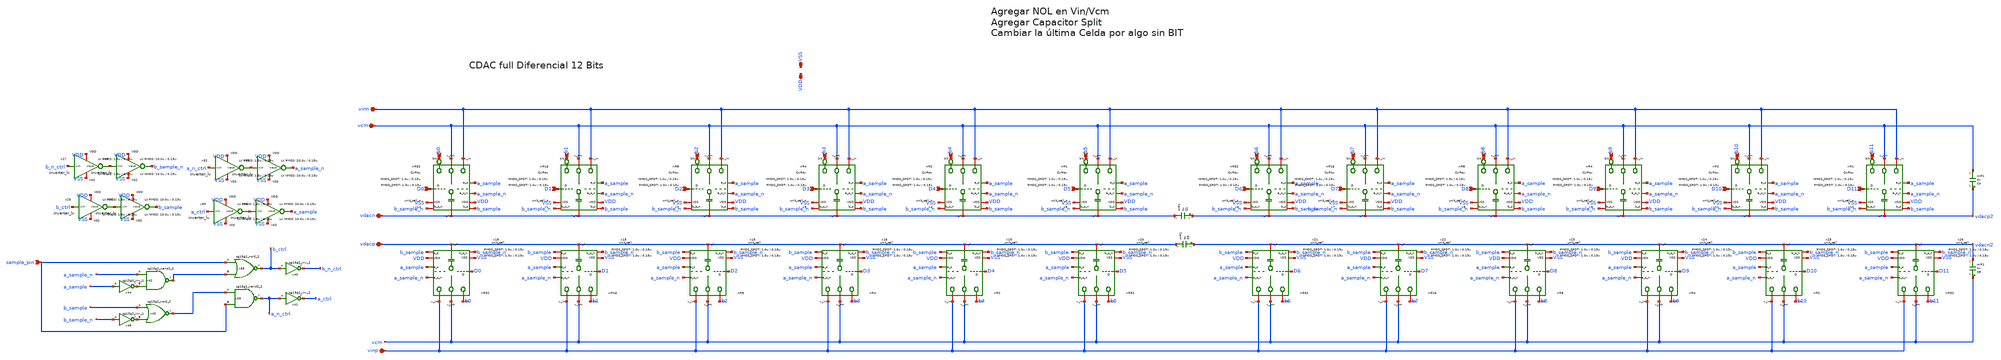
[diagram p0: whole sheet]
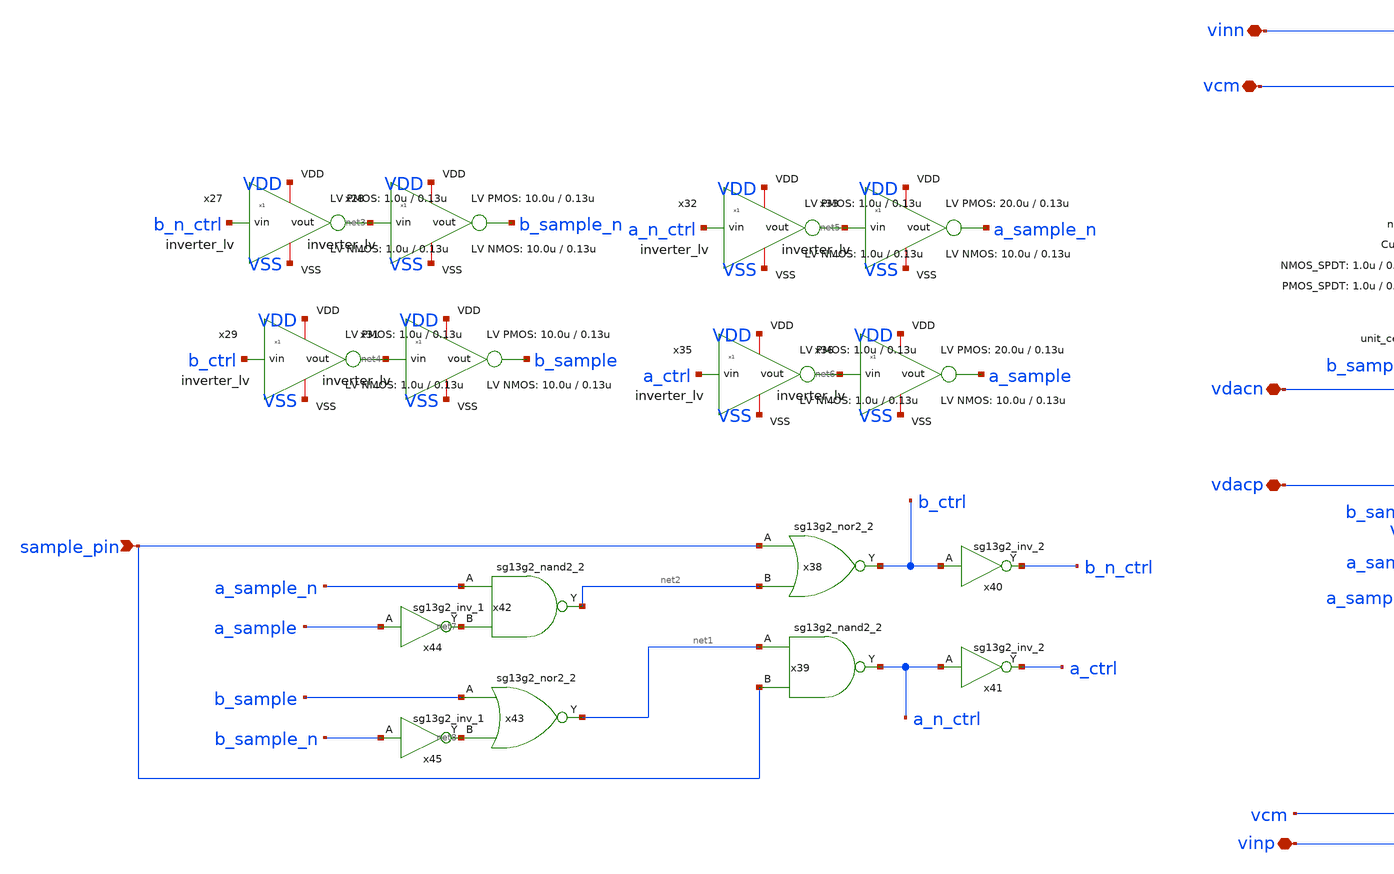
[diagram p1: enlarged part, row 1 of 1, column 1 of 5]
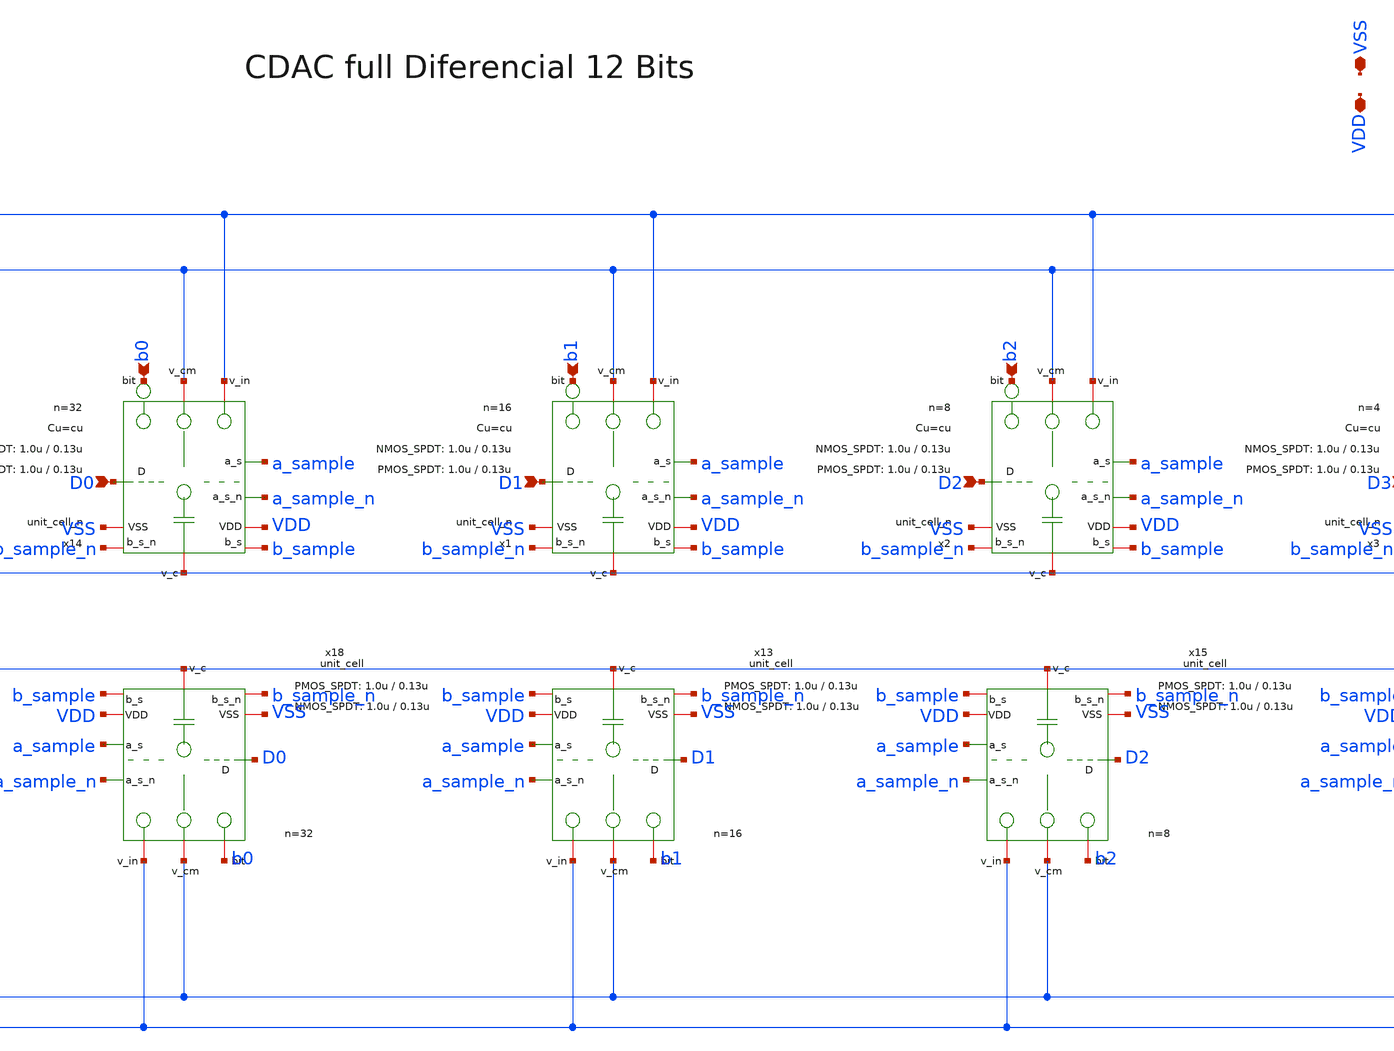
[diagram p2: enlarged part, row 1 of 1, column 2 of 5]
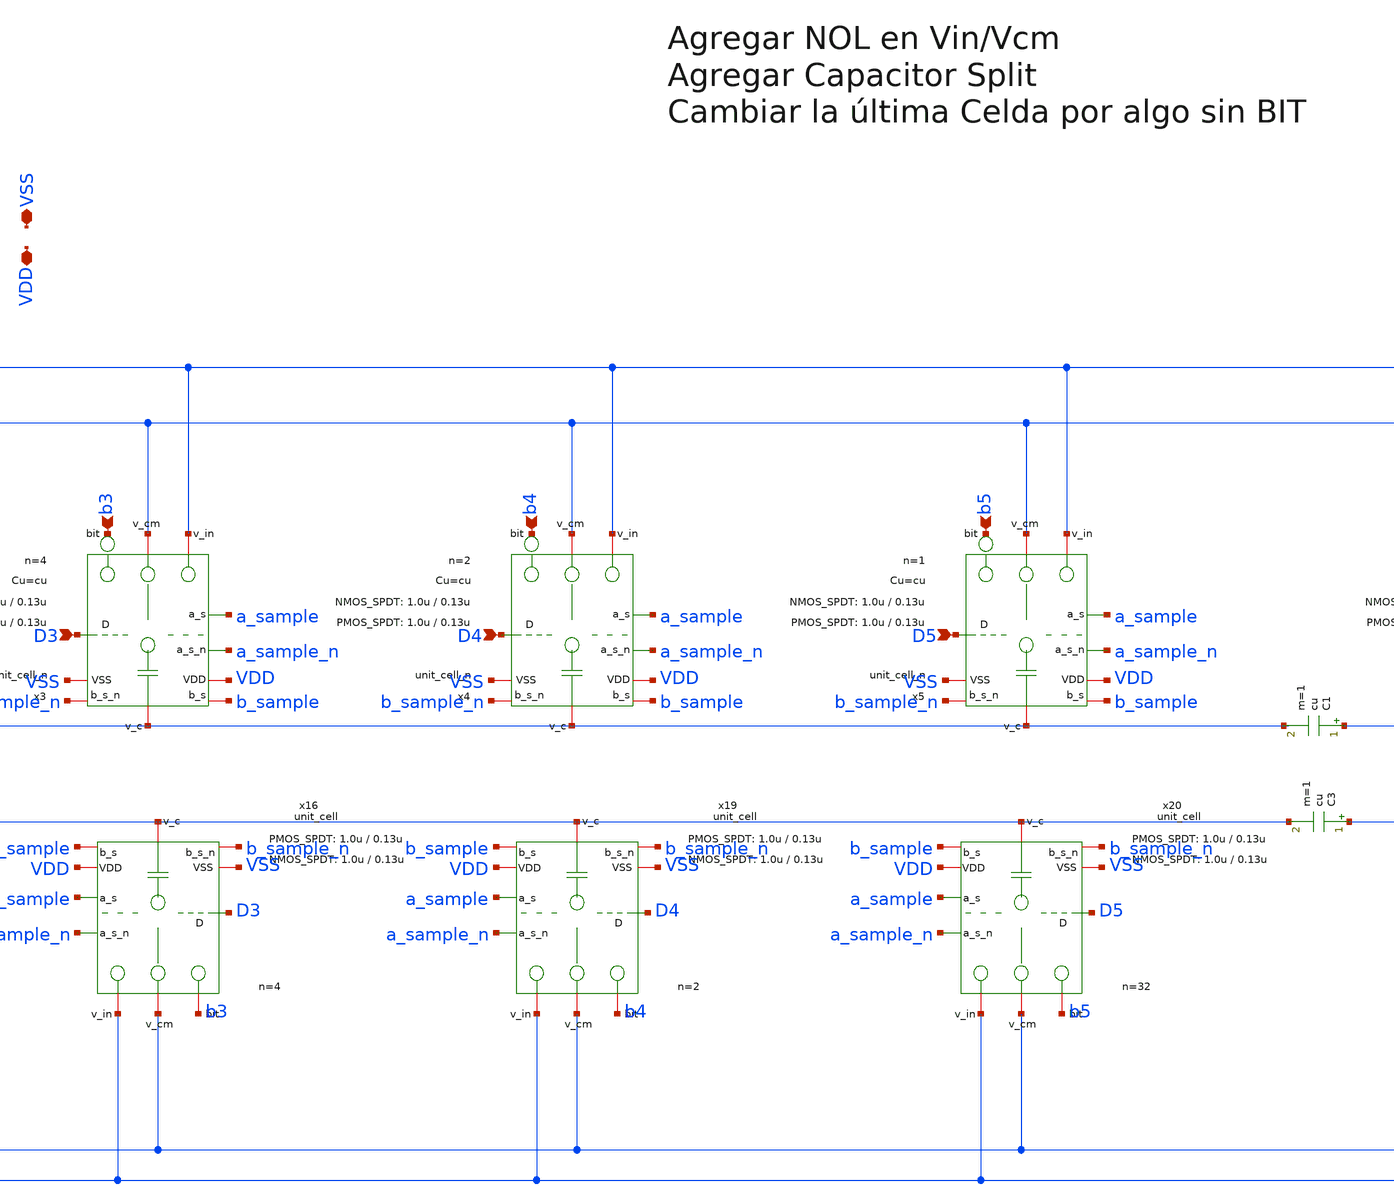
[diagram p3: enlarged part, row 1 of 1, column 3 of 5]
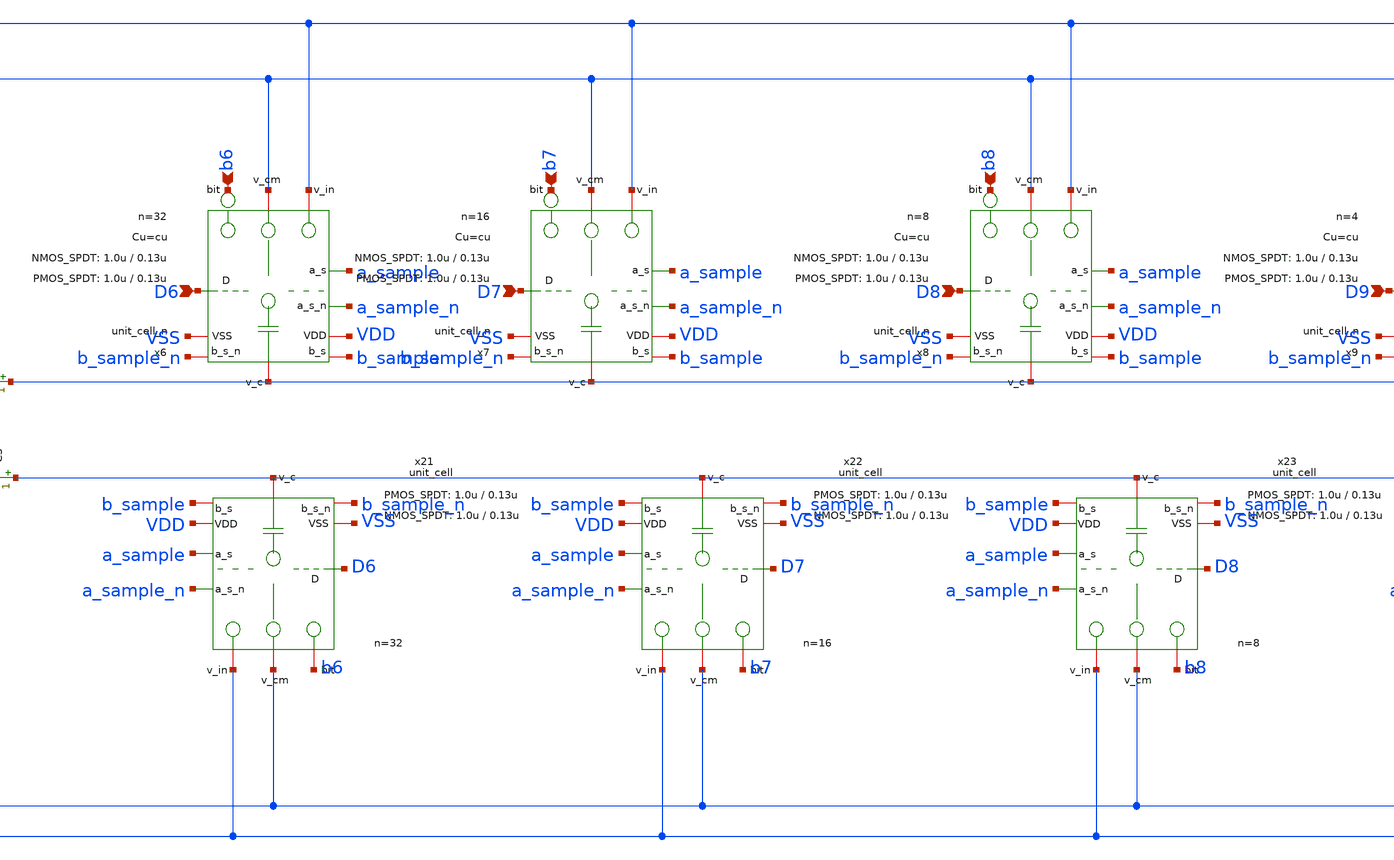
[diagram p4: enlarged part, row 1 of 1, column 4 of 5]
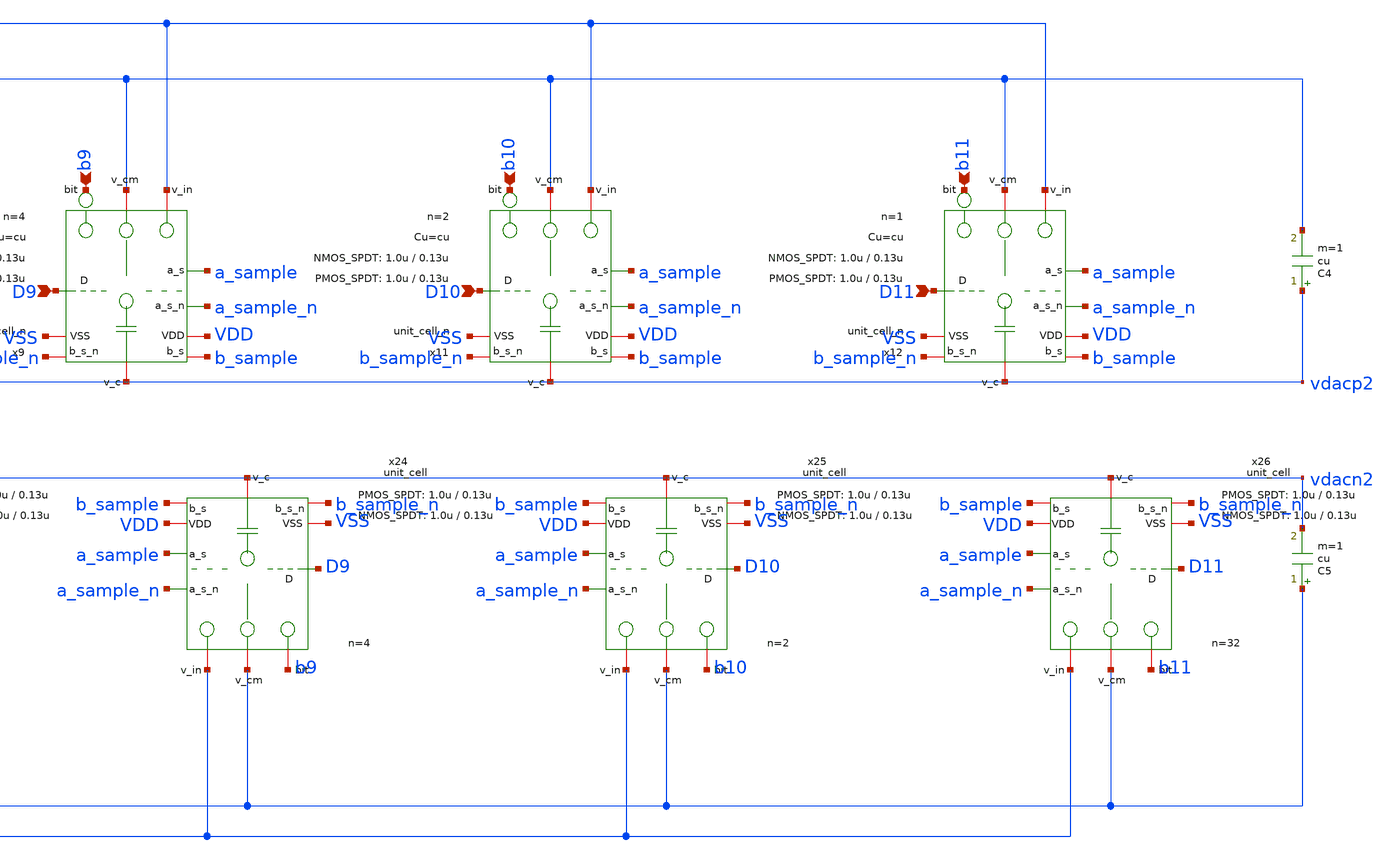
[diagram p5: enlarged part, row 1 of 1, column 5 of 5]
** sch_path: xschem/dac_icms_cell_ideal/dac.sch
* IHP-GmbH/IHP-Open-PDK/ihp-sg13g2/libs.tech/xschem/sg13g2_stdcells/sg13g2_inv_2.sch:
* Copyright 2023 IHP PDK Authors
* Licensed under the Apache License, Version 2.0 (the "License");
**.subckt dac D0 b0 vinp vcm sample_pin vinn vdacp vdacn VSS VDD D1 b1 D2 b2 D3 b3 D4 b4 D5 b5 D6 b6
*+ D7 b7 D8 b8 D9 b9 D10 b10 D11 b11
*.ipin D0
*.ipin b0
*.iopin vinp
*.iopin vcm
*.ipin sample_pin
*.iopin vinn
*.iopin vdacp
*.iopin vdacn
*.iopin VSS
*.iopin VDD
*.ipin D1
*.ipin b1
*.ipin D2
*.ipin b2
*.ipin D3
*.ipin b3
*.ipin D4
*.ipin b4
*.ipin D5
*.ipin b5
*.ipin D6
*.ipin b6
*.ipin D7
*.ipin b7
*.ipin D8
*.ipin b8
*.ipin D9
*.ipin b9
*.ipin D10
*.ipin b10
*.ipin D11
*.ipin b11
x14 VDD D0 VSS vdacn b0 vcm vinn a_sample a_sample_n b_sample b_sample_n unit_cell_n W_P=
+ L_P_SPDT=0.13u W_N= L_N_SPDT=0.13u Cu=cu n=32
x18 VDD D0 VSS vdacp b0 vcm vinp a_sample a_sample_n b_sample b_sample_n unit_cell W_P_SPDT=1.0u
+ L_P_SPDT=0.13u W_N_SPDT=1.0u L_N_SPDT=0.13u Cu=cu n=32
C1 vdacp2 vdacn cu m=1
C4 vdacp2 vcm cu m=1
x1 VDD D1 VSS vdacn b1 vcm vinn a_sample a_sample_n b_sample b_sample_n unit_cell_n W_P=
+ L_P_SPDT=0.13u W_N= L_N_SPDT=0.13u Cu=cu n=16
x2 VDD D2 VSS vdacn b2 vcm vinn a_sample a_sample_n b_sample b_sample_n unit_cell_n W_P=
+ L_P_SPDT=0.13u W_N= L_N_SPDT=0.13u Cu=cu n=8
x3 VDD D3 VSS vdacn b3 vcm vinn a_sample a_sample_n b_sample b_sample_n unit_cell_n W_P=
+ L_P_SPDT=0.13u W_N= L_N_SPDT=0.13u Cu=cu n=4
x4 VDD D4 VSS vdacn b4 vcm vinn a_sample a_sample_n b_sample b_sample_n unit_cell_n W_P=
+ L_P_SPDT=0.13u W_N= L_N_SPDT=0.13u Cu=cu n=2
x5 VDD D5 VSS vdacn b5 vcm vinn a_sample a_sample_n b_sample b_sample_n unit_cell_n W_P=
+ L_P_SPDT=0.13u W_N= L_N_SPDT=0.13u Cu=cu n=1
x6 VDD D6 VSS vdacp2 b6 vcm vinn a_sample a_sample_n b_sample b_sample_n unit_cell_n W_P=
+ L_P_SPDT=0.13u W_N= L_N_SPDT=0.13u Cu=cu n=32
x7 VDD D7 VSS vdacp2 b7 vcm vinn a_sample a_sample_n b_sample b_sample_n unit_cell_n W_P=
+ L_P_SPDT=0.13u W_N= L_N_SPDT=0.13u Cu=cu n=16
x8 VDD D8 VSS vdacp2 b8 vcm vinn a_sample a_sample_n b_sample b_sample_n unit_cell_n W_P=
+ L_P_SPDT=0.13u W_N= L_N_SPDT=0.13u Cu=cu n=8
x9 VDD D9 VSS vdacp2 b9 vcm vinn a_sample a_sample_n b_sample b_sample_n unit_cell_n W_P=
+ L_P_SPDT=0.13u W_N= L_N_SPDT=0.13u Cu=cu n=4
x11 VDD D10 VSS vdacp2 b10 vcm vinn a_sample a_sample_n b_sample b_sample_n unit_cell_n W_P=
+ L_P_SPDT=0.13u W_N= L_N_SPDT=0.13u Cu=cu n=2
x12 VDD D11 VSS vdacp2 b11 vcm vinn a_sample a_sample_n b_sample b_sample_n unit_cell_n W_P=
+ L_P_SPDT=0.13u W_N= L_N_SPDT=0.13u Cu=cu n=1
x13 VDD D1 VSS vdacp b1 vcm vinp a_sample a_sample_n b_sample b_sample_n unit_cell W_P_SPDT=1.0u
+ L_P_SPDT=0.13u W_N_SPDT=1.0u L_N_SPDT=0.13u Cu=cu n=16
x15 VDD D2 VSS vdacp b2 vcm vinp a_sample a_sample_n b_sample b_sample_n unit_cell W_P_SPDT=1.0u
+ L_P_SPDT=0.13u W_N_SPDT=1.0u L_N_SPDT=0.13u Cu=cu n=8
x16 VDD D3 VSS vdacp b3 vcm vinp a_sample a_sample_n b_sample b_sample_n unit_cell W_P_SPDT=1.0u
+ L_P_SPDT=0.13u W_N_SPDT=1.0u L_N_SPDT=0.13u Cu=cu n=4
x19 VDD D4 VSS vdacp b4 vcm vinp a_sample a_sample_n b_sample b_sample_n unit_cell W_P_SPDT=1.0u
+ L_P_SPDT=0.13u W_N_SPDT=1.0u L_N_SPDT=0.13u Cu=cu n=2
x20 VDD D5 VSS vdacp b5 vcm vinp a_sample a_sample_n b_sample b_sample_n unit_cell W_P_SPDT=1.0u
+ L_P_SPDT=0.13u W_N_SPDT=1.0u L_N_SPDT=0.13u Cu=cu n=32
C3 vdacn2 vdacp cu m=1
x21 VDD D6 VSS vdacn2 b6 vcm vinp a_sample a_sample_n b_sample b_sample_n unit_cell W_P_SPDT=1.0u
+ L_P_SPDT=0.13u W_N_SPDT=1.0u L_N_SPDT=0.13u Cu=cu n=32
x22 VDD D7 VSS vdacn2 b7 vcm vinp a_sample a_sample_n b_sample b_sample_n unit_cell W_P_SPDT=1.0u
+ L_P_SPDT=0.13u W_N_SPDT=1.0u L_N_SPDT=0.13u Cu=cu n=16
x23 VDD D8 VSS vdacn2 b8 vcm vinp a_sample a_sample_n b_sample b_sample_n unit_cell W_P_SPDT=1.0u
+ L_P_SPDT=0.13u W_N_SPDT=1.0u L_N_SPDT=0.13u Cu=cu n=8
x24 VDD D9 VSS vdacn2 b9 vcm vinp a_sample a_sample_n b_sample b_sample_n unit_cell W_P_SPDT=1.0u
+ L_P_SPDT=0.13u W_N_SPDT=1.0u L_N_SPDT=0.13u Cu=cu n=4
x25 VDD D10 VSS vdacn2 b10 vcm vinp a_sample a_sample_n b_sample b_sample_n unit_cell W_P_SPDT=1.0u
+ L_P_SPDT=0.13u W_N_SPDT=1.0u L_N_SPDT=0.13u Cu=cu n=2
x26 VDD D11 VSS vdacn2 b11 vcm vinp a_sample a_sample_n b_sample b_sample_n unit_cell W_P_SPDT=1.0u
+ L_P_SPDT=0.13u W_N_SPDT=1.0u L_N_SPDT=0.13u Cu=cu n=32
C5 vcm vdacn2 cu m=1
x27 VDD b_n_ctrl net3 VSS inverter_lv W_P=1.0u L_P=0.13u W_N=1.0u L_N=0.13u N_C=1
x28 VDD net3 b_sample_n VSS inverter_lv W_P=10.0u L_P=0.13u W_N=10.0u L_N=0.13u N_C=1
x29 VDD b_ctrl net4 VSS inverter_lv W_P=1.0u L_P=0.13u W_N=1.0u L_N=0.13u N_C=1
x31 VDD net4 b_sample VSS inverter_lv W_P=10.0u L_P=0.13u W_N=10.0u L_N=0.13u N_C=1
x32 VDD a_n_ctrl net5 VSS inverter_lv W_P=1.0u L_P=0.13u W_N=1.0u L_N=0.13u N_C=1
x33 VDD net5 a_sample_n VSS inverter_lv W_P=20.0u L_P=0.13u W_N=10.0u L_N=0.13u N_C=1
x35 VDD a_ctrl net6 VSS inverter_lv W_P=1.0u L_P=0.13u W_N=1.0u L_N=0.13u N_C=1
x36 VDD net6 a_sample VSS inverter_lv W_P=20.0u L_P=0.13u W_N=10.0u L_N=0.13u N_C=1
x38 b_ctrl sample_pin net2 VDD VSS sg13g2_nor2_2
x39 a_n_ctrl net1 sample_pin VDD VSS sg13g2_nand2_2
x40 b_n_ctrl b_ctrl VDD VSS sg13g2_inv_2
x41 a_ctrl a_n_ctrl VDD VSS sg13g2_inv_2
x42 net2 a_sample_n net7 VDD VSS sg13g2_nand2_2
x43 net1 b_sample net8 VDD VSS sg13g2_nor2_2
x44 net7 a_sample VDD VSS sg13g2_inv_1
x45 net8 b_sample_n VDD VSS sg13g2_inv_1
**.ends

* expanding   symbol:  dac_icms_cell/unit_cell_n.sym # of pins=11
** sym_path: xschem/dac_icms_cell/unit_cell_n.sym
** sch_path: xschem/dac_icms_cell/unit_cell_n.sch
.subckt unit_cell_n VDD d VSS v_top bit v_cm v_in a_sample a_sample_n b_sample b_sample_n
+  W_P_SPDT=1.0u L_P_SPDT=0.13u W_N_SPDT=1.0u L_N_SPDT=0.13u Cu=8f n=1
*.iopin VSS
*.iopin v_in
*.ipin d
*.ipin bit
*.iopin v_top
*.iopin v_cm
*.ipin b_sample
*.ipin b_sample_n
*.ipin a_sample
*.ipin a_sample_n
*.iopin VDD
S1 net2 net3 d VSS SW1
C2 net1 v_top Cu m=n
S2 net3 net1 b_sample b_sample_n SW1
S3 v_in net1 b_sample_n b_sample SW1
S4 v_top v_cm a_sample a_sample_n SW1
S5 VDD net2 bit VSS SW1
S6 net2 VSS bitn VSS SW1
S7 net3 v_cm dn VSS SW1
x8 VDD bit bitn VSS inverter_lv W_P=W_P_SPDT L_P=L_P_SPDT W_N=W_N_SPDT L_N=L_N_SPDT N_C=1
x1 VDD d dn VSS inverter_lv W_P=W_P_SPDT L_P=L_P_SPDT W_N=W_N_SPDT L_N=L_N_SPDT N_C=1
.ends


* expanding   symbol:  dac_icms_cell/unit_cell.sym # of pins=11
** sym_path: xschem/dac_icms_cell/unit_cell.sym
** sch_path: xschem/dac_icms_cell/unit_cell.sch
.subckt unit_cell VDD d VSS v_top bit v_cm v_in a_sample a_sample_n b_sample b_sample_n
+  W_P_SPDT=1.0u L_P_SPDT=0.13u W_N_SPDT=1.0u L_N_SPDT=0.13u Cu=8f n=1
*.iopin VSS
*.iopin v_in
*.ipin d
*.ipin bit
*.iopin v_top
*.iopin v_cm
*.ipin b_sample
*.ipin b_sample_n
*.ipin a_sample
*.ipin a_sample_n
*.iopin VDD
S7 net2 net3 d VSS SW1
C1 net1 v_top Cu m=n
S9 net3 net1 b_sample b_sample_n SW1
S10 v_in net1 b_sample_n b_sample SW1
S11 v_top v_cm a_sample a_sample_n SW1
S12 VSS net2 bit VSS SW1
S13 net2 VDD bitn VSS SW1
S14 net3 v_cm dn VSS SW1
x8 VDD bit bitn VSS inverter_lv W_P=W_P_SPDT L_P=L_P_SPDT W_N=W_N_SPDT L_N=L_N_SPDT N_C=1
x1 VDD d dn VSS inverter_lv W_P=W_P_SPDT L_P=L_P_SPDT W_N=W_N_SPDT L_N=L_N_SPDT N_C=1
.ends


* expanding   symbol:  inverter/inverter_lv.sym # of pins=4
** sym_path: xschem/inverter/inverter_lv.sym
** sch_path: xschem/inverter/inverter_lv.sch
.subckt inverter_lv VDD vin vout VSS  W_P=3.0u L_P=0.13u W_N=1.0u L_N=0.13u N_C=1
*.ipin vin
*.iopin VDD
*.iopin VSS
*.opin vout
XM1 vout vin VDD VDD sg13_lv_pmos w=W_P l=L_P ng=1 m={N_C} mm_ok=1
XM2 vout vin VSS VSS sg13_lv_nmos w=W_N l=L_N ng=1 m={N_C} mm_ok=1
.ends


* expanding   symbol:  sg13g2_stdcells/sg13g2_nor2_2.sym # of pins=3
** sym_path: sg13g2_stdcells/sg13g2_nor2_2.sym
** sch_path: sg13g2_stdcells/sg13g2_nor2_2.sch
.subckt sg13g2_nor2_2 Y A B VDD VSS
*.opin Y
*.ipin B
*.ipin A
*.iopin VDD
*.iopin VSS
XM1 Y A VSS VSS sg13_lv_nmos w=1.48u l=130.00n ng=2 m=1 mm_ok=1
XM2 Y B VSS VSS sg13_lv_nmos w=1.48u l=130.00n ng=2 m=1 mm_ok=1
XM3 net1 A VDD VDD sg13_lv_pmos w=2.24u l=130.00n ng=2 m=1 mm_ok=1
XM4 Y B net1 VDD sg13_lv_pmos w=2.24u l=130.00n ng=2 m=1 mm_ok=1
.ends


* expanding   symbol:  sg13g2_stdcells/sg13g2_nand2_2.sym # of pins=3
** sym_path: sg13g2_stdcells/sg13g2_nand2_2.sym
** sch_path: sg13g2_stdcells/sg13g2_nand2_2.sch
.subckt sg13g2_nand2_2 Y A B VDD VSS
*.iopin VDD
*.iopin VSS
*.opin Y
*.ipin B
*.ipin A
XM1 Y A net1 VSS sg13_lv_nmos w=1.44u l=130.00n ng=2 m=1 mm_ok=1
XM2 net1 B VSS VSS sg13_lv_nmos w=1.44u l=130.00n ng=2 m=1 mm_ok=1
XM3 Y A VDD VDD sg13_lv_pmos w=2.24u l=130.00n ng=2 m=1 mm_ok=1
XM4 Y B VDD VDD sg13_lv_pmos w=2.24u l=130.00n ng=2 m=1 mm_ok=1
.ends


* expanding   symbol:  sg13g2_stdcells/sg13g2_inv_2.sym # of pins=2
** sym_path: sg13g2_stdcells/sg13g2_inv_2.sym
** sch_path: sg13g2_stdcells/sg13g2_inv_2.sch
.subckt sg13g2_inv_2 Y A VDD VSS
*.opin Y
*.ipin A
*.iopin VDD
*.iopin VSS
XM1 Y A VSS VSS sg13_lv_nmos w=1.48u l=130.00n ng=2 m=1 mm_ok=1
XM2 Y A VDD VDD sg13_lv_pmos w=2.24u l=130.00n ng=2 m=1 mm_ok=1
.ends


* expanding   symbol:  sg13g2_stdcells/sg13g2_inv_1.sym # of pins=2
** sym_path: sg13g2_stdcells/sg13g2_inv_1.sym
** sch_path: sg13g2_stdcells/sg13g2_inv_1.sch
.subckt sg13g2_inv_1 Y A VDD VSS
*.opin Y
*.ipin A
*.iopin VDD
*.iopin VSS
XM1 Y A VSS VSS sg13_lv_nmos w=740.00n l=130.00n ng=1 m=1 mm_ok=1
XM2 Y A VDD VDD sg13_lv_pmos w=1.12u l=130.00n ng=1 m=1 mm_ok=1
.ends

**** begin user architecture code
.MODEL SW1 SW   VT=0.9 VH=0.01  RON=ro ROFF=10G
**** end user architecture code
.end
